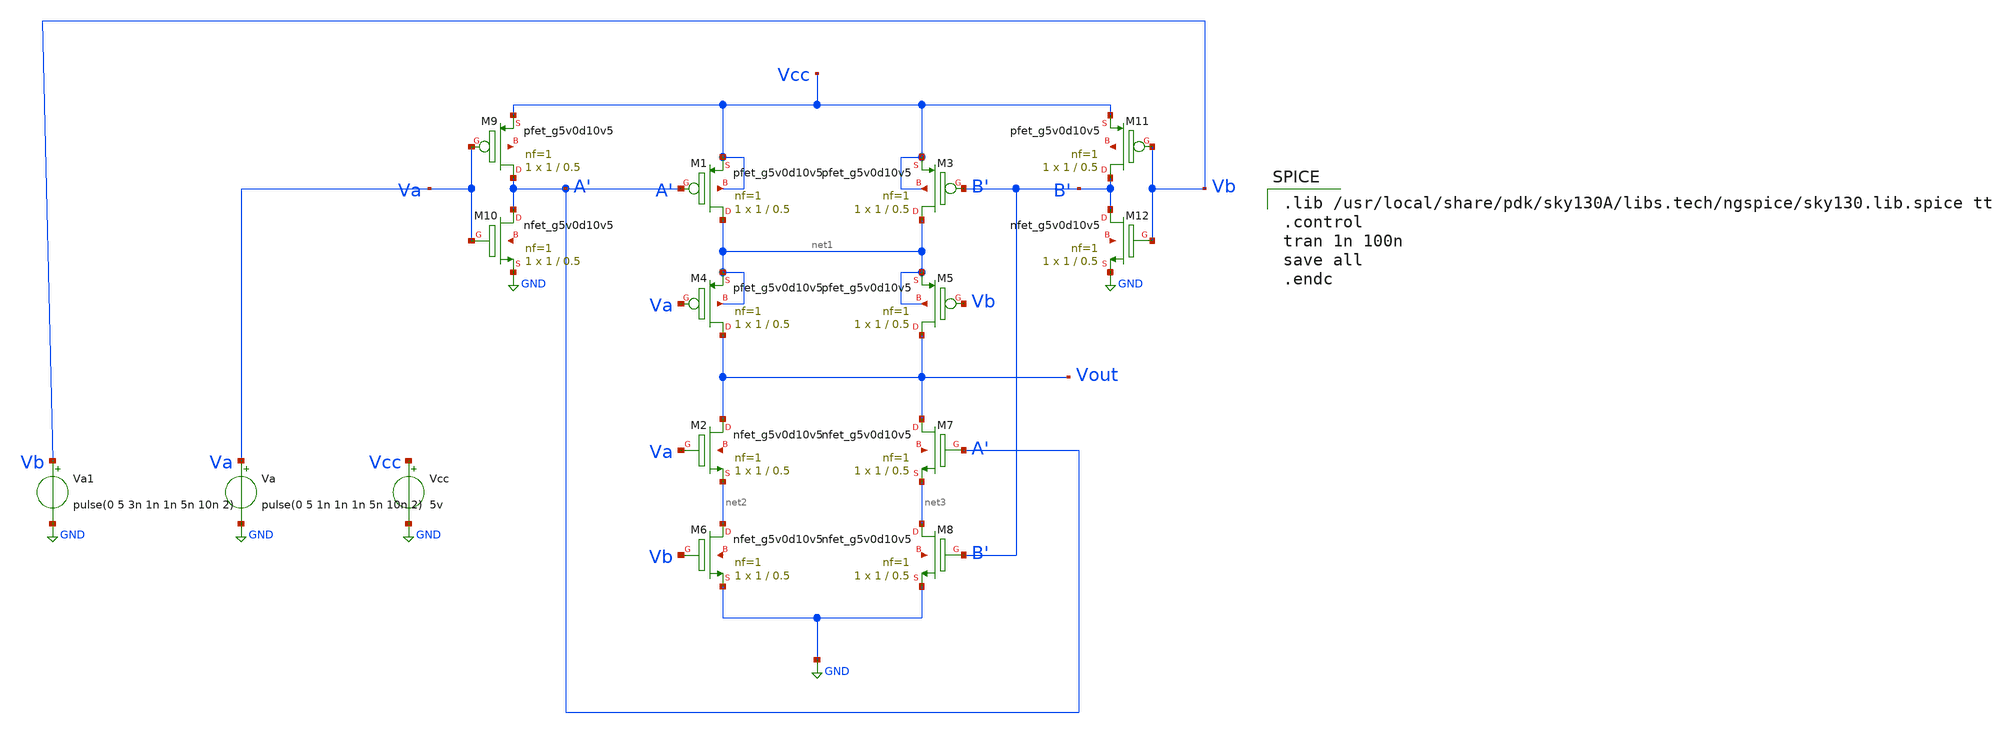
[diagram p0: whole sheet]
** sch_path: Schematic Simulation/trial2.sch
**.subckt trial2
Vcc Vcc GND 5v
Va Va GND pulse(0 5 1n 1n 1n 5n 10n 2)
XM1 net1 A' Vcc Vcc sky130_fd_pr__pfet_g5v0d10v5 L=0.5 W=1 nf=1 ad='int((nf+1)/2) * W/nf * 0.29' as='int((nf+2)/2)
+ * W/nf * 0.29' pd='2*int((nf+1)/2) * (W/nf + 0.29)' ps='2*int((nf+2)/2) * (W/nf + 0.29)' nrd='0.29 /
+ W' nrs='0.29 / W' sa=0 sb=0 sd=0 mult=1 m=1
XM2 Vout Va net2 net4 sky130_fd_pr__nfet_g5v0d10v5 L=0.5 W=1 nf=1 ad='int((nf+1)/2) * W/nf * 0.29' as='int((nf+2)/2)
+ * W/nf * 0.29' pd='2*int((nf+1)/2) * (W/nf + 0.29)' ps='2*int((nf+2)/2) * (W/nf + 0.29)' nrd='0.29 /
+ W' nrs='0.29 / W' sa=0 sb=0 sd=0 mult=1 m=1
XM3 net1 B' Vcc Vcc sky130_fd_pr__pfet_g5v0d10v5 L=0.5 W=1 nf=1 ad='int((nf+1)/2) * W/nf * 0.29' as='int((nf+2)/2) * W/nf * 0.29'
+ pd='2*int((nf+1)/2) * (W/nf + 0.29)' ps='2*int((nf+2)/2) * (W/nf + 0.29)' nrd='0.29 / W' nrs='0.29 / W'
+ sa=0 sb=0 sd=0 mult=1 m=1
XM4 Vout Va net1 net1 sky130_fd_pr__pfet_g5v0d10v5 L=0.5 W=1 nf=1 ad='int((nf+1)/2) * W/nf * 0.29' as='int((nf+2)/2) * W/nf * 0.29'
+ pd='2*int((nf+1)/2) * (W/nf + 0.29)' ps='2*int((nf+2)/2) * (W/nf + 0.29)' nrd='0.29 / W' nrs='0.29 / W'
+ sa=0 sb=0 sd=0 mult=1 m=1
XM5 Vout Vb net1 net1 sky130_fd_pr__pfet_g5v0d10v5 L=0.5 W=1 nf=1 ad='int((nf+1)/2) * W/nf * 0.29' as='int((nf+2)/2) * W/nf * 0.29'
+ pd='2*int((nf+1)/2) * (W/nf + 0.29)' ps='2*int((nf+2)/2) * (W/nf + 0.29)' nrd='0.29 / W' nrs='0.29 / W'
+ sa=0 sb=0 sd=0 mult=1 m=1
XM6 net2 Vb GND net5 sky130_fd_pr__nfet_g5v0d10v5 L=0.5 W=1 nf=1 ad='int((nf+1)/2) * W/nf * 0.29' as='int((nf+2)/2) * W/nf * 0.29'
+ pd='2*int((nf+1)/2) * (W/nf + 0.29)' ps='2*int((nf+2)/2) * (W/nf + 0.29)' nrd='0.29 / W' nrs='0.29 / W'
+ sa=0 sb=0 sd=0 mult=1 m=1
XM7 Vout A' net3 net6 sky130_fd_pr__nfet_g5v0d10v5 L=0.5 W=1 nf=1 ad='int((nf+1)/2) * W/nf * 0.29' as='int((nf+2)/2)
+ * W/nf * 0.29' pd='2*int((nf+1)/2) * (W/nf + 0.29)' ps='2*int((nf+2)/2) * (W/nf + 0.29)' nrd='0.29 /
+ W' nrs='0.29 / W' sa=0 sb=0 sd=0 mult=1 m=1
XM8 net3 B' GND net7 sky130_fd_pr__nfet_g5v0d10v5 L=0.5 W=1 nf=1 ad='int((nf+1)/2) * W/nf * 0.29' as='int((nf+2)/2) * W/nf * 0.29'
+ pd='2*int((nf+1)/2) * (W/nf + 0.29)' ps='2*int((nf+2)/2) * (W/nf + 0.29)' nrd='0.29 / W' nrs='0.29 / W'
+ sa=0 sb=0 sd=0 mult=1 m=1
XM9 A' Va Vcc net8 sky130_fd_pr__pfet_g5v0d10v5 L=0.5 W=1 nf=1 ad='int((nf+1)/2) * W/nf * 0.29' as='int((nf+2)/2)
+ * W/nf * 0.29' pd='2*int((nf+1)/2) * (W/nf + 0.29)' ps='2*int((nf+2)/2) * (W/nf + 0.29)' nrd='0.29 /
+ W' nrs='0.29 / W' sa=0 sb=0 sd=0 mult=1 m=1
XM10 A' Va GND net9 sky130_fd_pr__nfet_g5v0d10v5 L=0.5 W=1 nf=1 ad='int((nf+1)/2) * W/nf * 0.29' as='int((nf+2)/2) * W/nf * 0.29'
+ pd='2*int((nf+1)/2) * (W/nf + 0.29)' ps='2*int((nf+2)/2) * (W/nf + 0.29)' nrd='0.29 / W' nrs='0.29 / W'
+ sa=0 sb=0 sd=0 mult=1 m=1
XM11 B' Vb Vcc net10 sky130_fd_pr__pfet_g5v0d10v5 L=0.5 W=1 nf=1 ad='int((nf+1)/2) * W/nf * 0.29' as='int((nf+2)/2)
+ * W/nf * 0.29' pd='2*int((nf+1)/2) * (W/nf + 0.29)' ps='2*int((nf+2)/2) * (W/nf + 0.29)' nrd='0.29 /
+ W' nrs='0.29 / W' sa=0 sb=0 sd=0 mult=1 m=1
XM12 B' Vb GND net11 sky130_fd_pr__nfet_g5v0d10v5 L=0.5 W=1 nf=1 ad='int((nf+1)/2) * W/nf * 0.29' as='int((nf+2)/2) * W/nf * 0.29'
+ pd='2*int((nf+1)/2) * (W/nf + 0.29)' ps='2*int((nf+2)/2) * (W/nf + 0.29)' nrd='0.29 / W' nrs='0.29 / W'
+ sa=0 sb=0 sd=0 mult=1 m=1
Va1 Vb GND pulse(0 5 3n 1n 1n 5n 10n 2)
**** begin user architecture code

.lib /usr/local/share/pdk/sky130A/libs.tech/ngspice/sky130.lib.spice tt
.control
tran 1n 100n
save all
.endc

**** end user architecture code
**.ends
.GLOBAL GND
.end
